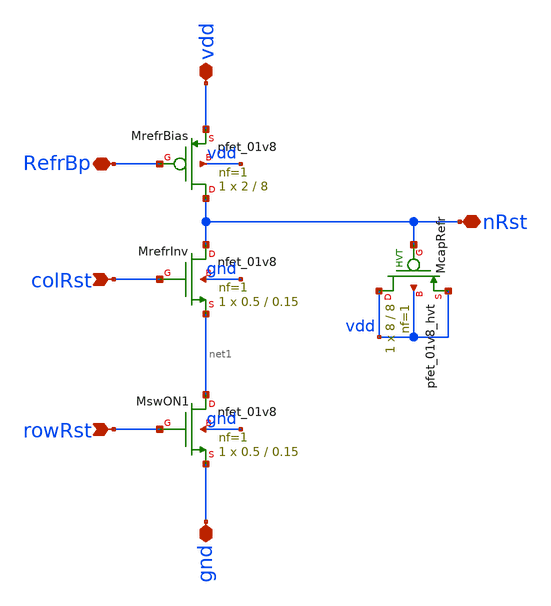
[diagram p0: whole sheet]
** sch_path: analog/xschem/PixelResetGen.sch
**.subckt PixelResetGen rowRst colRst RefrBp gnd vdd nRst
*.ipin rowRst
*.ipin colRst
*.iopin RefrBp
*.iopin gnd
*.iopin vdd
*.iopin nRst
XMrefrInv nRst colRst net1 gnd sky130_fd_pr__nfet_01v8 L=0.15 W=0.5 nf=1 ad='int((1 + 1)/2) * 0.5 / 1 * 0.29'
+ as='int((1 + 2)/2) * 0.5 / 1 * 0.29' pd='2*int((1 + 1)/2) * (0.5 / 1 + 0.29)' ps='2*int((1 + 2)/2) * (0.5 / 1 + 0.29)'
+ nrd='0.29 / 0.5 ' nrs='0.29 / 0.5 ' sa=0 sb=0 sd=0 mult=1 m=1
XMrefrBias nRst RefrBp vdd vdd sky130_fd_pr__pfet_01v8 L=8 W=2 nf=1 ad='int((1 + 1)/2) * 2 / 1 * 0.29'
+ as='int((1 + 2)/2) * 2 / 1 * 0.29' pd='2*int((1 + 1)/2) * (2 / 1 + 0.29)' ps='2*int((1 + 2)/2) * (2 / 1 + 0.29)'
+ nrd='0.29 / 2 ' nrs='0.29 / 2 ' sa=0 sb=0 sd=0 mult=1 m=1
XMcapRefr vdd nRst vdd vdd sky130_fd_pr__pfet_01v8_hvt L=8 W=8 nf=1 ad='int((1 + 1)/2) * 8 / 1 * 0.29'
+ as='int((1 + 2)/2) * 8 / 1 * 0.29' pd='2*int((1 + 1)/2) * (8 / 1 + 0.29)' ps='2*int((1 + 2)/2) * (8 / 1 + 0.29)'
+ nrd='0.29 / 8 ' nrs='0.29 / 8 ' sa=0 sb=0 sd=0 mult=1 m=1
XMswON1 net1 rowRst gnd gnd sky130_fd_pr__nfet_01v8 L=0.15 W=0.5 nf=1 ad='int((1 + 1)/2) * 0.5 / 1 * 0.29'
+ as='int((1 + 2)/2) * 0.5 / 1 * 0.29' pd='2*int((1 + 1)/2) * (0.5 / 1 + 0.29)' ps='2*int((1 + 2)/2) * (0.5 / 1 + 0.29)'
+ nrd='0.29 / 0.5 ' nrs='0.29 / 0.5 ' sa=0 sb=0 sd=0 mult=1 m=1
**.ends
.end
